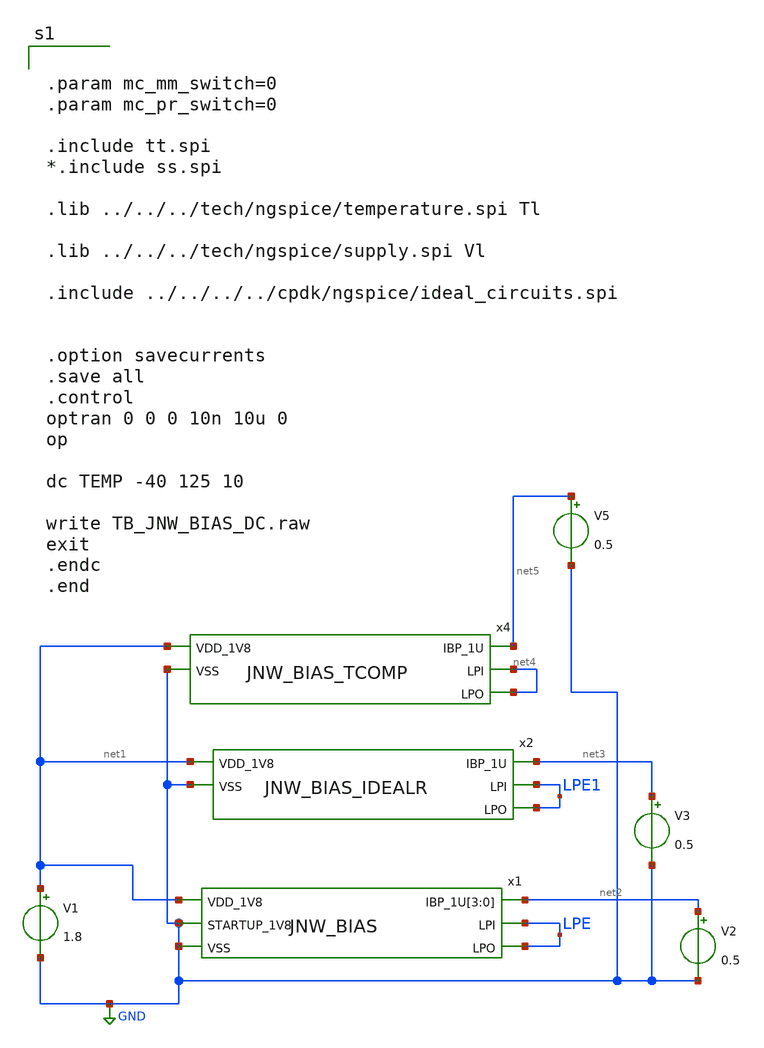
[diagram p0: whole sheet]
** sch_path: design/JNW_BIAS_SKY130A/TB_JNW_BIAS_DC.sch
**.subckt TB_JNW_BIAS_DC
x1 net1 LPE net2 net2 net2 net2 LPE GND GND JNW_BIAS
V1 net1 GND 1.8
V2 net2 GND 0.5
x2 net1 net3 LPE1 LPE1 GND JNW_BIAS_IDEALR
V3 net3 GND 0.5
x4 net1 net5 net4 net4 GND JNW_BIAS_TCOMP
V5 net5 GND 0.5
**** begin user architecture code


.param mc_mm_switch=0
.param mc_pr_switch=0

.include tt.spi
*.include ss.spi

.lib ../../../tech/ngspice/temperature.spi Tl

.lib ../../../tech/ngspice/supply.spi Vl

.include ../../../../cpdk/ngspice/ideal_circuits.spi


.option savecurrents
.save all
.control
optran 0 0 0 10n 10u 0
op

dc TEMP -40 125 10

write TB_JNW_BIAS_DC.raw
exit
.endc
.end



**** end user architecture code
**.ends
.GLOBAL GND
.end
